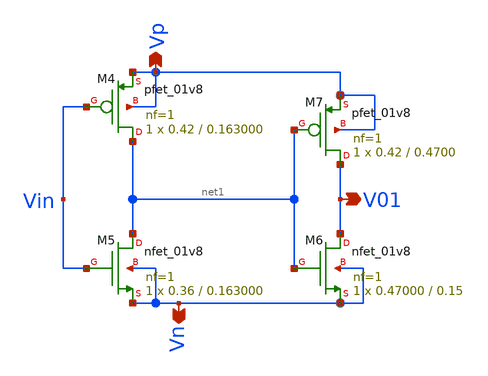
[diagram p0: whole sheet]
** sch_path: xschem/Vth_sch/Symbol/th1_2.sch
**.subckt th1_2 Vn Vp V01
*.opin Vn
*.opin Vp
*.opin V01
XM7 V01 net1 Vp Vp sky130_fd_pr__pfet_01v8 L=0.4700 W=0.42 nf=1 ad='int((nf+1)/2) * W/nf * 0.29' as='int((nf+2)/2) * W/nf * 0.29'
+ pd='2*int((nf+1)/2) * (W/nf + 0.29)' ps='2*int((nf+2)/2) * (W/nf + 0.29)' nrd='0.29 / W' nrs='0.29 / W'
+ sa=0 sb=0 sd=0 mult=1 m=1
XM6 V01 net1 Vn Vn sky130_fd_pr__nfet_01v8 L=0.15 W=0.47000 nf=1 ad='int((nf+1)/2) * W/nf * 0.29' as='int((nf+2)/2) * W/nf * 0.29'
+ pd='2*int((nf+1)/2) * (W/nf + 0.29)' ps='2*int((nf+2)/2) * (W/nf + 0.29)' nrd='0.29 / W' nrs='0.29 / W'
+ sa=0 sb=0 sd=0 mult=1 m=1
XM4 net1 Vin Vp Vp sky130_fd_pr__pfet_01v8 L=0.163000 W=0.42 nf=1 ad='int((nf+1)/2) * W/nf * 0.29' as='int((nf+2)/2) * W/nf * 0.29'
+ pd='2*int((nf+1)/2) * (W/nf + 0.29)' ps='2*int((nf+2)/2) * (W/nf + 0.29)' nrd='0.29 / W' nrs='0.29 / W'
+ sa=0 sb=0 sd=0 mult=1 m=1
XM5 net1 Vin Vn Vn sky130_fd_pr__nfet_01v8 L=0.163000 W=0.36 nf=1 ad='int((nf+1)/2) * W/nf * 0.29' as='int((nf+2)/2) * W/nf * 0.29'
+ pd='2*int((nf+1)/2) * (W/nf + 0.29)' ps='2*int((nf+2)/2) * (W/nf + 0.29)' nrd='0.29 / W' nrs='0.29 / W'
+ sa=0 sb=0 sd=0 mult=1 m=1
**.ends
.end
